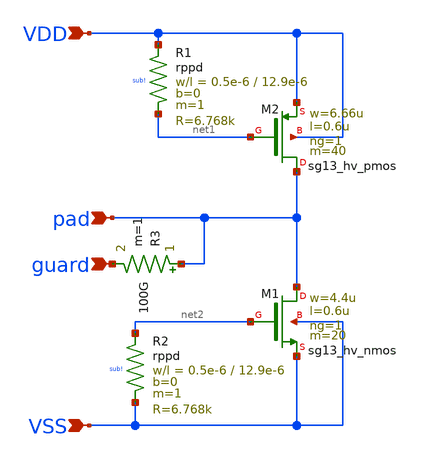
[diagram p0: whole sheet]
** sch_path: trident_test_structures/design_data/xschem/clamps.sch
**.subckt clamps VDD VSS pad guard
*.ipin VDD
*.ipin VSS
*.ipin pad
*.ipin guard
XM1 pad net2 VSS VSS sg13_hv_nmos w=4.4u l=0.6u ng=1 m=20 mm_ok=1
XR1 VDD net1 sub! rppd w=0.5e-6 l=12.9e-6 m=1 b=0 mm_ok=1
XM2 pad net1 VDD VDD sg13_hv_pmos w=6.66u l=0.6u ng=1 m=40 mm_ok=1
XR2 net2 VSS sub! rppd w=0.5e-6 l=12.9e-6 m=1 b=0 mm_ok=1
R3 pad guard 100G m=1
**.ends
.end
